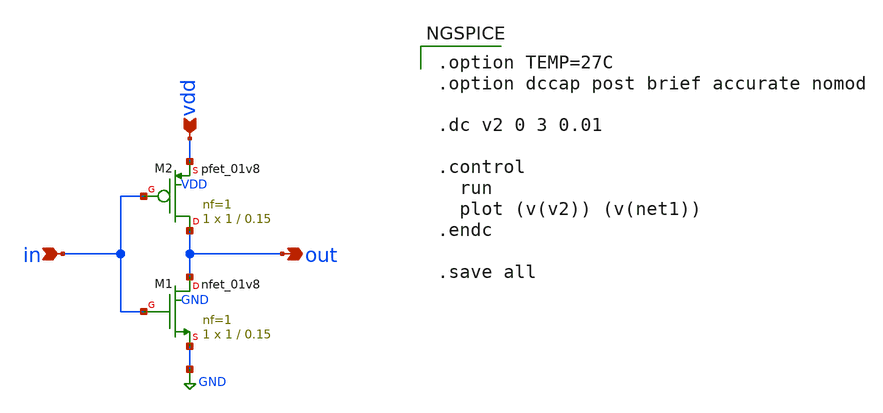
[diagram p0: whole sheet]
** sch_path: xschem/attenuator/invert.sch
**.subckt invert in out vdd
*.ipin in
*.opin out
*.ipin vdd
XM1 out in GND GND sky130_fd_pr__nfet_01v8 L=0.15 W=1 nf=1 ad='int((nf+1)/2) * W/nf * 0.29' as='int((nf+2)/2) * W/nf * 0.29'
+ pd='2*int((nf+1)/2) * (W/nf + 0.29)' ps='2*int((nf+2)/2) * (W/nf + 0.29)' nrd='0.29 / W' nrs='0.29 / W'
+ sa=0 sb=0 sd=0 mult=1 m=1
XM2 out in vdd VDD sky130_fd_pr__pfet_01v8 L=0.15 W=1 nf=1 ad='int((nf+1)/2) * W/nf * 0.29' as='int((nf+2)/2) * W/nf * 0.29'
+ pd='2*int((nf+1)/2) * (W/nf + 0.29)' ps='2*int((nf+2)/2) * (W/nf + 0.29)' nrd='0.29 / W' nrs='0.29 / W'
+ sa=0 sb=0 sd=0 mult=1 m=1
**** begin user architecture code
 ** manual skywater pdks install (with patches applied)
* .lib $::SKYWATER_MODELS/models/sky130.lib.spice tt

** opencircuitdesign pdks install
.lib $::SKYWATER_MODELS/sky130.lib.spice tt

.param mc_mm_switch=0
.param mc_pr_switch=0


.option TEMP=27C
.option dccap post brief accurate nomod

.dc v2 0 3 0.01

.control
  run
  plot (v(v2)) (v(net1))
.endc

.save all


**** end user architecture code
**.ends
.GLOBAL GND
.end
